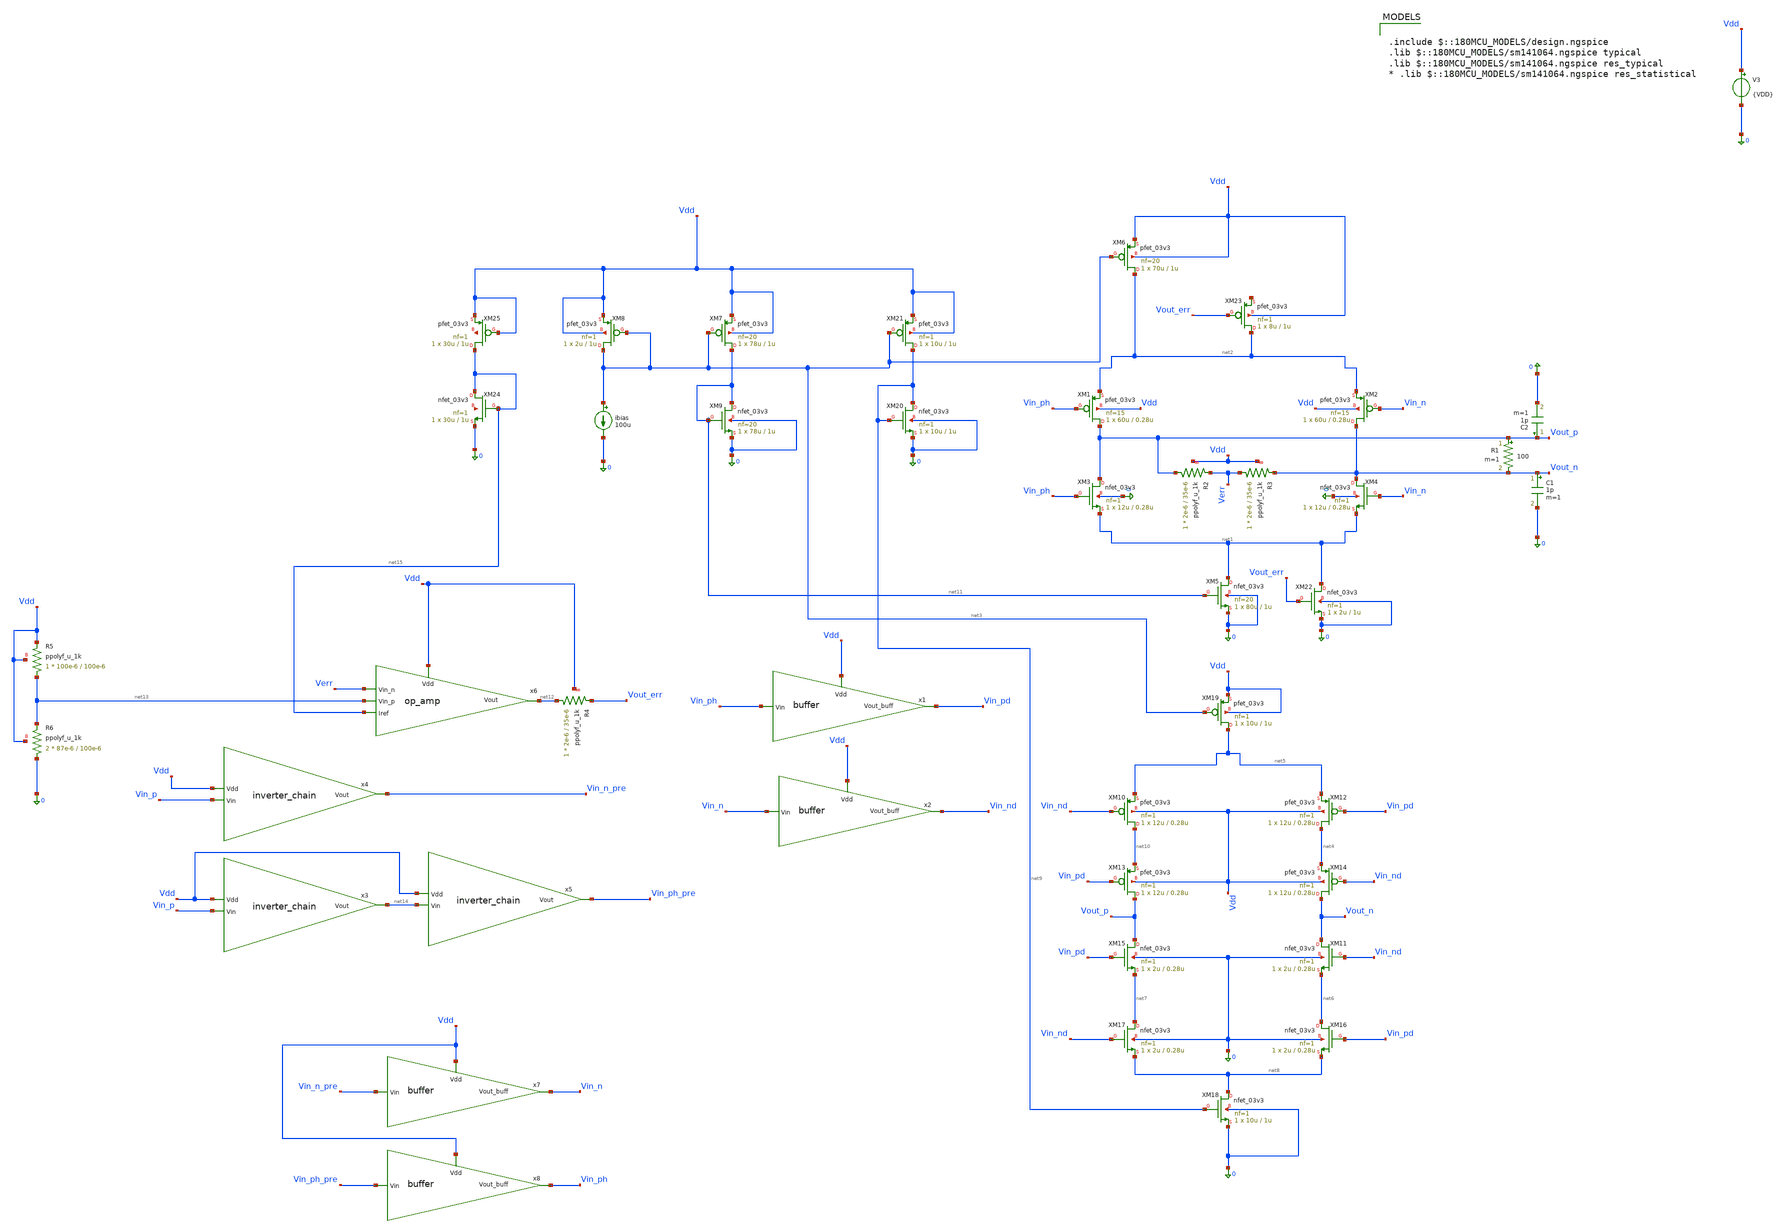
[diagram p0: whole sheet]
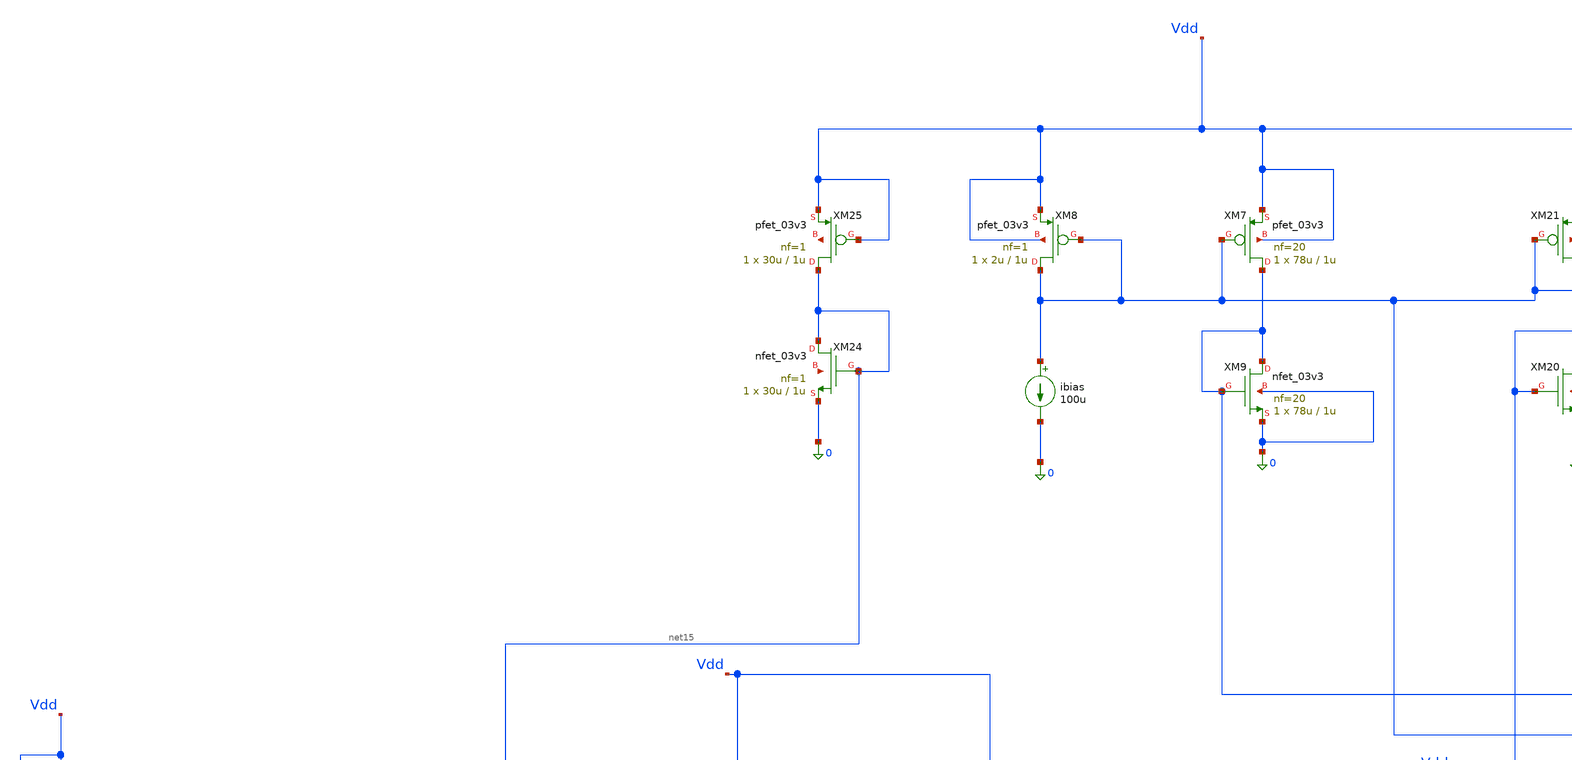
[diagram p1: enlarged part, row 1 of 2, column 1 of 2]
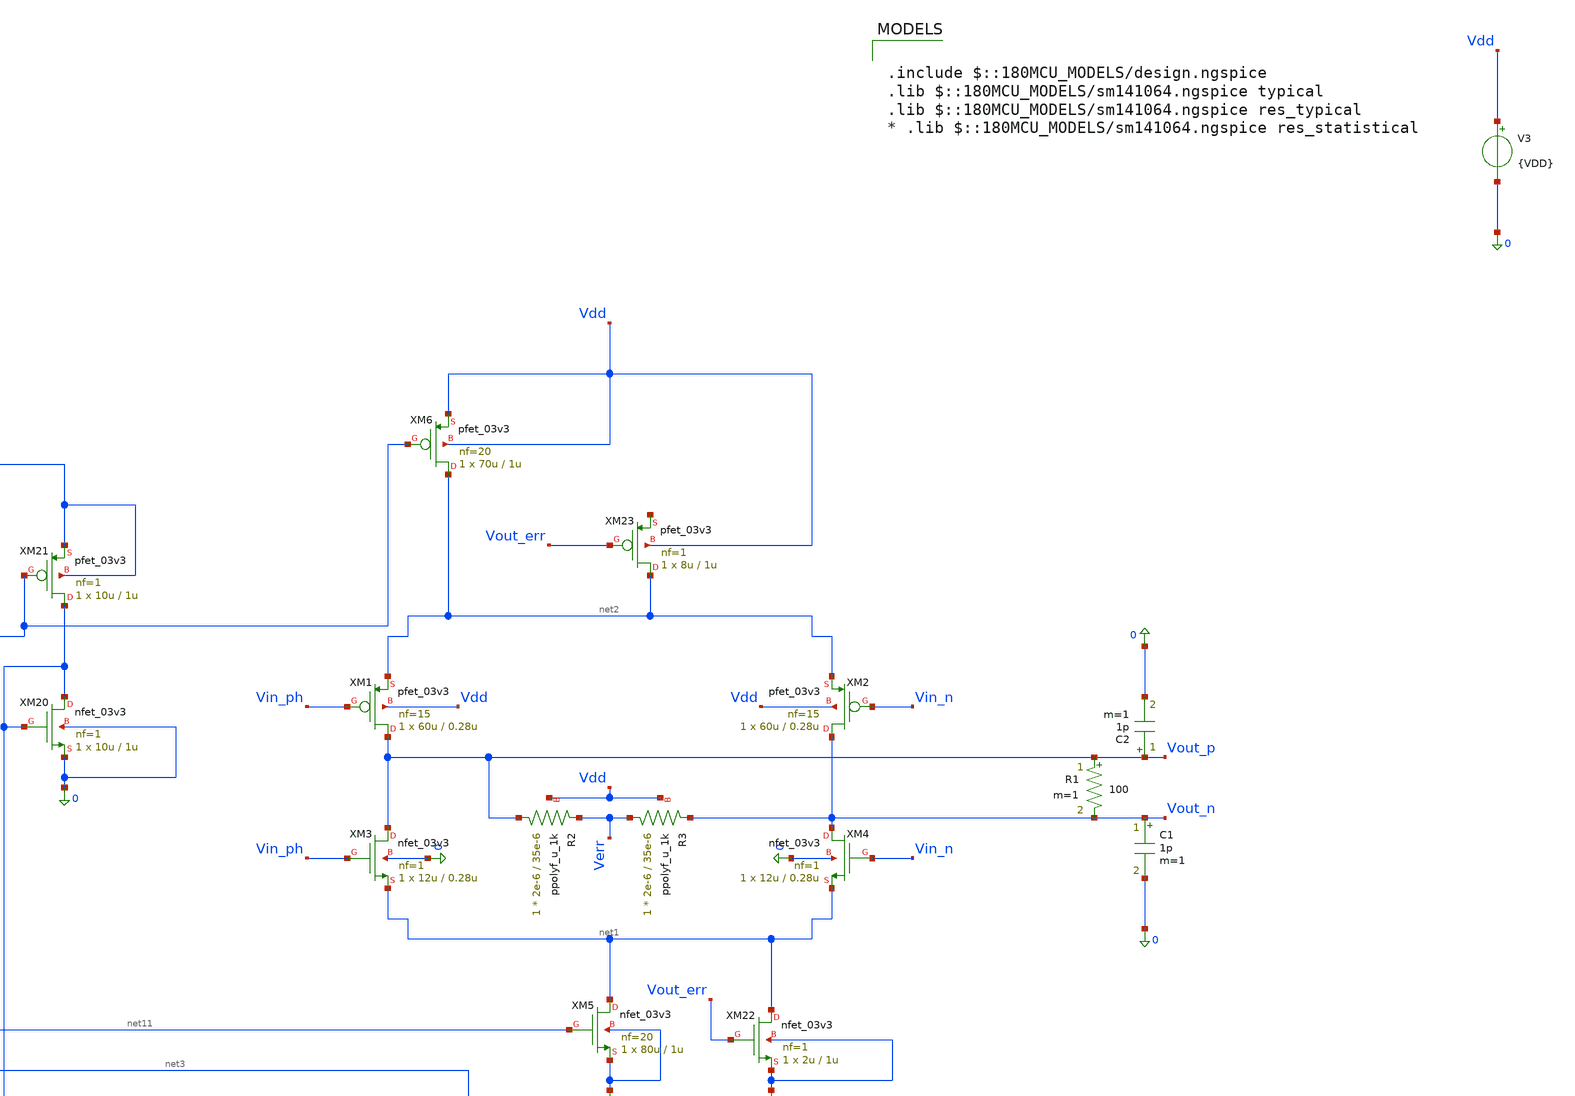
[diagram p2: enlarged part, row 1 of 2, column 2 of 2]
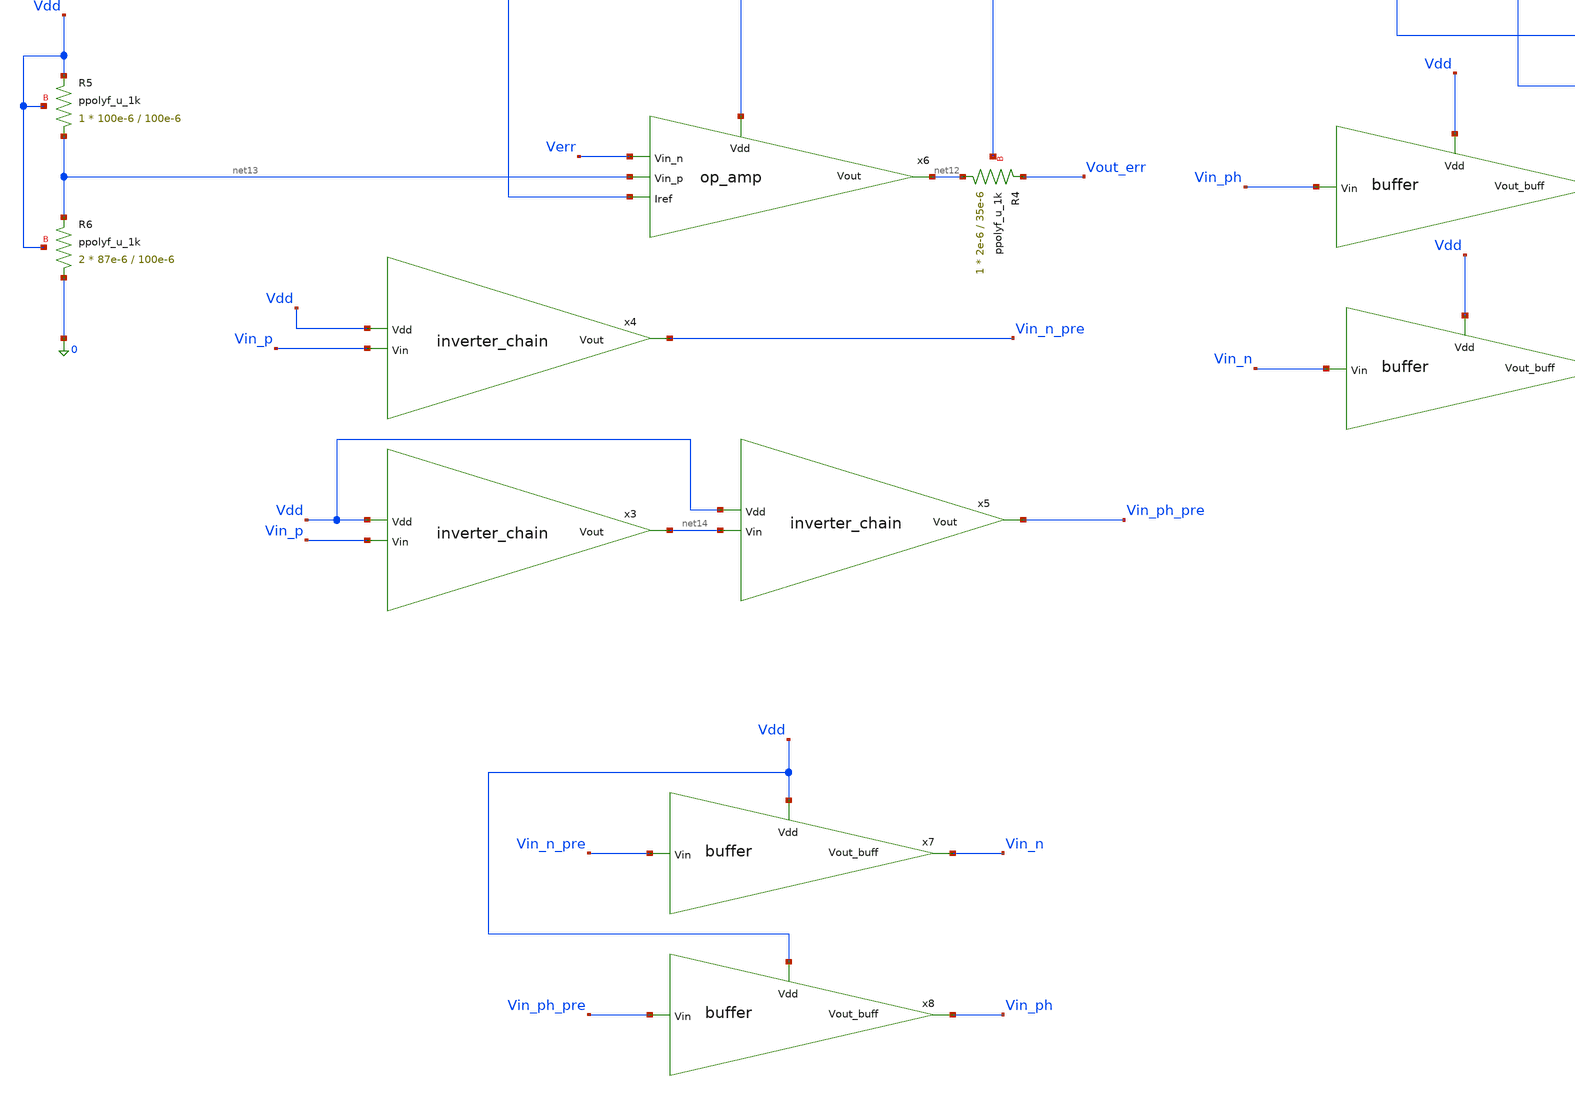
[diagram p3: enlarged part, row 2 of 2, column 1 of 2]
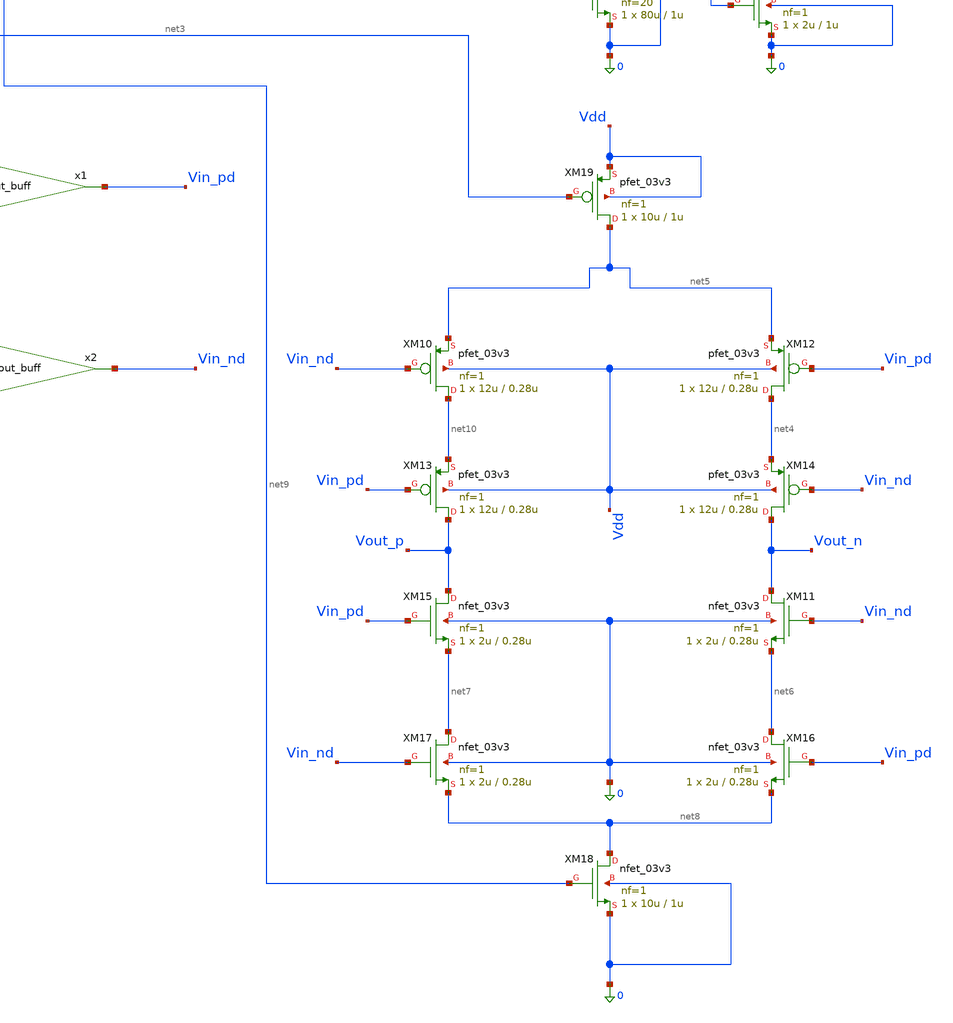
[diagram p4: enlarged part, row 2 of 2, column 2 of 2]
** sch_path: blocks/adc/lvds/lvds_testing.sch
**.subckt lvds_testing
R1 Vout_p Vout_n 100 m=1
V3 Vdd 0 {VDD}
XM1 Vout_p Vin_ph net2 Vdd pfet_03v3 L=0.28u W=60u nf=15 ad='int((nf+1)/2) * W/nf * 0.18u' as='int((nf+2)/2) * W/nf * 0.18u'
+ pd='2*int((nf+1)/2) * (W/nf + 0.18u)' ps='2*int((nf+2)/2) * (W/nf + 0.18u)' nrd='0.18u / W' nrs='0.18u / W'
+ sa=0 sb=0 sd=0 m=1
XM2 Vout_n Vin_n net2 Vdd pfet_03v3 L=0.28u W=60u nf=15 ad='int((nf+1)/2) * W/nf * 0.18u' as='int((nf+2)/2) * W/nf * 0.18u'
+ pd='2*int((nf+1)/2) * (W/nf + 0.18u)' ps='2*int((nf+2)/2) * (W/nf + 0.18u)' nrd='0.18u / W' nrs='0.18u / W'
+ sa=0 sb=0 sd=0 m=1
XM3 Vout_p Vin_ph net1 0 nfet_03v3 L=0.28u W=12u nf=1 ad='int((nf+1)/2) * W/nf * 0.18u' as='int((nf+2)/2) * W/nf * 0.18u'
+ pd='2*int((nf+1)/2) * (W/nf + 0.18u)' ps='2*int((nf+2)/2) * (W/nf + 0.18u)' nrd='0.18u / W' nrs='0.18u / W'
+ sa=0 sb=0 sd=0 m=1
XM4 Vout_n Vin_n net1 0 nfet_03v3 L=0.28u W=12u nf=1 ad='int((nf+1)/2) * W/nf * 0.18u' as='int((nf+2)/2) * W/nf * 0.18u'
+ pd='2*int((nf+1)/2) * (W/nf + 0.18u)' ps='2*int((nf+2)/2) * (W/nf + 0.18u)' nrd='0.18u / W' nrs='0.18u / W'
+ sa=0 sb=0 sd=0 m=1
XM5 net1 net11 0 0 nfet_03v3 L=1u W=80u nf=20 ad='int((nf+1)/2) * W/nf * 0.18u' as='int((nf+2)/2) * W/nf * 0.18u'
+ pd='2*int((nf+1)/2) * (W/nf + 0.18u)' ps='2*int((nf+2)/2) * (W/nf + 0.18u)' nrd='0.18u / W' nrs='0.18u / W'
+ sa=0 sb=0 sd=0 m=1
XM6 net2 net3 Vdd Vdd pfet_03v3 L=1u W=70u nf=20 ad='int((nf+1)/2) * W/nf * 0.18u' as='int((nf+2)/2) * W/nf * 0.18u'
+ pd='2*int((nf+1)/2) * (W/nf + 0.18u)' ps='2*int((nf+2)/2) * (W/nf + 0.18u)' nrd='0.18u / W' nrs='0.18u / W'
+ sa=0 sb=0 sd=0 m=1
XM8 net3 net3 Vdd Vdd pfet_03v3 L=1u W=2u nf=1 ad='int((nf+1)/2) * W/nf * 0.18u' as='int((nf+2)/2) * W/nf * 0.18u'
+ pd='2*int((nf+1)/2) * (W/nf + 0.18u)' ps='2*int((nf+2)/2) * (W/nf + 0.18u)' nrd='0.18u / W' nrs='0.18u / W'
+ sa=0 sb=0 sd=0 m=1
ibias net3 0 100u
XM10 net10 Vin_nd net5 Vdd pfet_03v3 L=0.28u W=12u nf=1 ad='int((nf+1)/2) * W/nf * 0.18u' as='int((nf+2)/2) * W/nf * 0.18u'
+ pd='2*int((nf+1)/2) * (W/nf + 0.18u)' ps='2*int((nf+2)/2) * (W/nf + 0.18u)' nrd='0.18u / W' nrs='0.18u / W'
+ sa=0 sb=0 sd=0 m=1
XM11 Vout_n Vin_nd net6 0 nfet_03v3 L=0.28u W=2u nf=1 ad='int((nf+1)/2) * W/nf * 0.18u' as='int((nf+2)/2) * W/nf * 0.18u'
+ pd='2*int((nf+1)/2) * (W/nf + 0.18u)' ps='2*int((nf+2)/2) * (W/nf + 0.18u)' nrd='0.18u / W' nrs='0.18u / W'
+ sa=0 sb=0 sd=0 m=1
XM12 net4 Vin_pd net5 Vdd pfet_03v3 L=0.28u W=12u nf=1 ad='int((nf+1)/2) * W/nf * 0.18u' as='int((nf+2)/2) * W/nf * 0.18u'
+ pd='2*int((nf+1)/2) * (W/nf + 0.18u)' ps='2*int((nf+2)/2) * (W/nf + 0.18u)' nrd='0.18u / W' nrs='0.18u / W'
+ sa=0 sb=0 sd=0 m=1
XM13 Vout_p Vin_pd net10 Vdd pfet_03v3 L=0.28u W=12u nf=1 ad='int((nf+1)/2) * W/nf * 0.18u' as='int((nf+2)/2) * W/nf * 0.18u'
+ pd='2*int((nf+1)/2) * (W/nf + 0.18u)' ps='2*int((nf+2)/2) * (W/nf + 0.18u)' nrd='0.18u / W' nrs='0.18u / W'
+ sa=0 sb=0 sd=0 m=1
XM14 Vout_n Vin_nd net4 Vdd pfet_03v3 L=0.28u W=12u nf=1 ad='int((nf+1)/2) * W/nf * 0.18u' as='int((nf+2)/2) * W/nf * 0.18u'
+ pd='2*int((nf+1)/2) * (W/nf + 0.18u)' ps='2*int((nf+2)/2) * (W/nf + 0.18u)' nrd='0.18u / W' nrs='0.18u / W'
+ sa=0 sb=0 sd=0 m=1
XM15 Vout_p Vin_pd net7 0 nfet_03v3 L=0.28u W=2u nf=1 ad='int((nf+1)/2) * W/nf * 0.18u' as='int((nf+2)/2) * W/nf * 0.18u'
+ pd='2*int((nf+1)/2) * (W/nf + 0.18u)' ps='2*int((nf+2)/2) * (W/nf + 0.18u)' nrd='0.18u / W' nrs='0.18u / W'
+ sa=0 sb=0 sd=0 m=1
XM16 net6 Vin_pd net8 0 nfet_03v3 L=0.28u W=2u nf=1 ad='int((nf+1)/2) * W/nf * 0.18u' as='int((nf+2)/2) * W/nf * 0.18u'
+ pd='2*int((nf+1)/2) * (W/nf + 0.18u)' ps='2*int((nf+2)/2) * (W/nf + 0.18u)' nrd='0.18u / W' nrs='0.18u / W'
+ sa=0 sb=0 sd=0 m=1
XM17 net7 Vin_nd net8 0 nfet_03v3 L=0.28u W=2u nf=1 ad='int((nf+1)/2) * W/nf * 0.18u' as='int((nf+2)/2) * W/nf * 0.18u'
+ pd='2*int((nf+1)/2) * (W/nf + 0.18u)' ps='2*int((nf+2)/2) * (W/nf + 0.18u)' nrd='0.18u / W' nrs='0.18u / W'
+ sa=0 sb=0 sd=0 m=1
XM18 net8 net9 0 0 nfet_03v3 L=1u W=10u nf=1 ad='int((nf+1)/2) * W/nf * 0.18u' as='int((nf+2)/2) * W/nf * 0.18u'
+ pd='2*int((nf+1)/2) * (W/nf + 0.18u)' ps='2*int((nf+2)/2) * (W/nf + 0.18u)' nrd='0.18u / W' nrs='0.18u / W'
+ sa=0 sb=0 sd=0 m=1
XM19 net5 net3 Vdd Vdd pfet_03v3 L=1u W=10u nf=1 ad='int((nf+1)/2) * W/nf * 0.18u' as='int((nf+2)/2) * W/nf * 0.18u'
+ pd='2*int((nf+1)/2) * (W/nf + 0.18u)' ps='2*int((nf+2)/2) * (W/nf + 0.18u)' nrd='0.18u / W' nrs='0.18u / W'
+ sa=0 sb=0 sd=0 m=1
XM21 net9 net3 Vdd Vdd pfet_03v3 L=1u W=10u nf=1 ad='int((nf+1)/2) * W/nf * 0.18u' as='int((nf+2)/2) * W/nf * 0.18u'
+ pd='2*int((nf+1)/2) * (W/nf + 0.18u)' ps='2*int((nf+2)/2) * (W/nf + 0.18u)' nrd='0.18u / W' nrs='0.18u / W'
+ sa=0 sb=0 sd=0 m=1
XM20 net9 net9 0 0 nfet_03v3 L=1u W=10u nf=1 ad='int((nf+1)/2) * W/nf * 0.18u' as='int((nf+2)/2) * W/nf * 0.18u'
+ pd='2*int((nf+1)/2) * (W/nf + 0.18u)' ps='2*int((nf+2)/2) * (W/nf + 0.18u)' nrd='0.18u / W' nrs='0.18u / W'
+ sa=0 sb=0 sd=0 m=1
C2 Vout_p 0 1p m=1
XR2 Vout_p Verr Vdd ppolyf_u_1k r_width=2e-6 r_length=35e-6 m=1
XR3 Verr Vout_n Vdd ppolyf_u_1k r_width=2e-6 r_length=35e-6 m=1
XM7 net11 net3 Vdd Vdd pfet_03v3 L=1u W=78u nf=20 ad='int((nf+1)/2) * W/nf * 0.18u' as='int((nf+2)/2) * W/nf * 0.18u'
+ pd='2*int((nf+1)/2) * (W/nf + 0.18u)' ps='2*int((nf+2)/2) * (W/nf + 0.18u)' nrd='0.18u / W' nrs='0.18u / W'
+ sa=0 sb=0 sd=0 m=1
XM9 net11 net11 0 0 nfet_03v3 L=1u W=78u nf=20 ad='int((nf+1)/2) * W/nf * 0.18u' as='int((nf+2)/2) * W/nf * 0.18u'
+ pd='2*int((nf+1)/2) * (W/nf + 0.18u)' ps='2*int((nf+2)/2) * (W/nf + 0.18u)' nrd='0.18u / W' nrs='0.18u / W'
+ sa=0 sb=0 sd=0 m=1
C1 Vout_n 0 1p m=1
x4 Vdd Vin_n_pre Vin_p inverter_chain
XM22 net1 Vout_err 0 0 nfet_03v3 L=1u W=2u nf=1 ad='int((nf+1)/2) * W/nf * 0.18u' as='int((nf+2)/2) * W/nf * 0.18u'
+ pd='2*int((nf+1)/2) * (W/nf + 0.18u)' ps='2*int((nf+2)/2) * (W/nf + 0.18u)' nrd='0.18u / W' nrs='0.18u / W'
+ sa=0 sb=0 sd=0 m=1
XM23 net2 Vout_err net16 Vdd pfet_03v3 L=1u W=8u nf=1 ad='int((nf+1)/2) * W/nf * 0.18u' as='int((nf+2)/2) * W/nf * 0.18u'
+ pd='2*int((nf+1)/2) * (W/nf + 0.18u)' ps='2*int((nf+2)/2) * (W/nf + 0.18u)' nrd='0.18u / W' nrs='0.18u / W'
+ sa=0 sb=0 sd=0 m=1
x3 Vdd net14 Vin_p inverter_chain
x5 Vdd Vin_ph_pre net14 inverter_chain
x7 Vdd Vin_n Vin_n_pre buffer
x8 Vdd Vin_ph Vin_ph_pre buffer
XM24 net15 net15 0 net17 nfet_03v3 L=1u W=30u nf=1 ad='int((nf+1)/2) * W/nf * 0.18u' as='int((nf+2)/2) * W/nf * 0.18u'
+ pd='2*int((nf+1)/2) * (W/nf + 0.18u)' ps='2*int((nf+2)/2) * (W/nf + 0.18u)' nrd='0.18u / W' nrs='0.18u / W'
+ sa=0 sb=0 sd=0 m=1
XM25 net15 Vdd Vdd net18 pfet_03v3 L=1u W=30u nf=1 ad='int((nf+1)/2) * W/nf * 0.18u' as='int((nf+2)/2) * W/nf * 0.18u'
+ pd='2*int((nf+1)/2) * (W/nf + 0.18u)' ps='2*int((nf+2)/2) * (W/nf + 0.18u)' nrd='0.18u / W' nrs='0.18u / W'
+ sa=0 sb=0 sd=0 m=1
x1 Vdd Vin_pd Vin_ph buffer
x2 Vdd Vin_nd Vin_n buffer
XR4 net12 Vout_err Vdd ppolyf_u_1k r_width=2e-6 r_length=35e-6 m=1
x6 Vdd net12 Verr net13 net15 op_amp
XR5 net13 Vdd Vdd ppolyf_u_1k r_width=100e-6 r_length=100e-6 m=1
XR6 0 net13 Vdd ppolyf_u_1k r_width=87e-6 r_length=100e-6 m=2
**** begin user architecture code


.param VDD=3.3
.param VCM=1.2

* Temperature parameter used by .options
.param TEMP=27
.options temp={TEMP}

* 2 Gbps
.param UI=500p
.param TR=20p
.param SEED=11

* Jitter setting
* Use 0p for no jitter, e.g. .param TJPP=0p
.param TJPP=0p

* ============================================================
* Internal pseudo-random data generation
* ============================================================

.func frac(x) {x - floor(x)}
.func rand01(n) {frac(sin((n + 1 + SEED)*12.9898)*43758.5453123)}
.func rand01j(n) {frac(sin((n + 1 + SEED)*78.233)*24634.6345)}
.func rbit(n) {floor(2*rand01(n))}
.func jitter(n) {(rand01j(n)-0.5)*TJPP}
.func edge(x) {0.5*(1 + tanh(x/(TR/10)))}
.func data_bit(t) {rbit(floor(t/UI)-1)+(rbit(floor(t/UI))-rbit(floor(t/UI)-1))*edge(t-floor(t/UI)*UI-jitter(floor(t/UI)))}

* ============================================================
* Behavioral input sources
* Remove/disable old PULSE sources connected to vin_p/vin_n.
* ============================================================

Bvinp vin_p 0 V={VDD*data_bit(time)}



.control
set filetype=ascii
set wr_singlescale
set numdgt=12

* Folder for output data files
shell rm /foss/designs/trans_testing/lvds_testing/lvds_eye_temp_m40.txt
shell rm /foss/designs/trans_testing/lvds_testing/lvds_eye_temp_27.txt
shell rm /foss/designs/trans_testing/lvds_testing/lvds_eye_temp_125.txt

* ============================================================
* Temperature = -40 C
* ============================================================

alterparam TEMP = -40
set temp=-40
reset
save v(vin_p) v(vin_n) v(vout_p) v(vout_n) v(Vin_ph) v(Vin_nd) v(Vin_pd) v(Vout_err)

tran 2p 200n 0 2p

let vod = v(vout_p)-v(vout_n)
let vcm_out = (v(vout_p)+v(vout_n))/2
let vod_abs = abs(vod)
let id_p = @m.xm5.m0[id]
let id_n = @m.xm6.m0[id]

plot v(Vin_n) v(Vin_nd)
plot v(Vin_pd) v(Vin_ph)
plot id_p id_n
plot v(Vout_err)


wrdata /foss/designs/trans_testing/lvds_testing/lvds_eye_temp_m40.txt v(vin_p) v(vin_n) v(vout_p)
+ v(vout_n) vod vcm_out


meas tran td_pd_rise TRIG v(vin_ph) VAL=1.65 RISE=10 TARG v(vin_pd) VAL=1.65 RISE=10
meas tran td_pd_fall TRIG v(vin_ph) VAL=1.65 FALL=10 TARG v(vin_pd) VAL=1.65 FALL=10

meas tran td_nd_rise TRIG v(vin_n) VAL=1.65 RISE=10 TARG v(vin_nd) VAL=1.65 RISE=10
meas tran td_nd_fall TRIG v(vin_n) VAL=1.65 FALL=10 TARG v(vin_nd) VAL=1.65 FALL=10

* 50% complementary skew
meas tran skew_ph_rise_n_fall TRIG v(vin_ph) VAL=1.65 RISE=10 TARG v(vin_n)  VAL=1.65 FALL=10
meas tran skew_ph_fall_n_rise TRIG v(vin_ph) VAL=1.65 FALL=10 TARG v(vin_n)  VAL=1.65 RISE=10

* Edge times
meas tran tr_ph TRIG v(vin_ph) VAL=0.33 RISE=10 TARG v(vin_ph) VAL=2.97 RISE=10
meas tran tf_ph TRIG v(vin_ph) VAL=2.97 FALL=10 TARG v(vin_ph) VAL=0.33 FALL=10

meas tran tr_n  TRIG v(vin_n)  VAL=0.33 RISE=10 TARG v(vin_n)  VAL=2.97 RISE=10
meas tran tf_n  TRIG v(vin_n)  VAL=2.97 FALL=10 TARG v(vin_n)  VAL=0.33 FALL=10
* ============================================================
* Temperature = 27 C
* ============================================================

alterparam TEMP = 27
set temp=27
reset
save v(vin_p) v(vin_n) v(vout_p) v(vout_n) v(Vin_ph) v(Vin_nd) v(Vin_pd) v(Vout_err)

tran 2p 200n 0 2p

let vod = v(vout_p)-v(vout_n)
let vcm_out = (v(vout_p)+v(vout_n))/2
let vod_abs = abs(vod)
let id_p = @m.xm5.m0[id]
let id_n = @m.xm6.m0[id]
plot v(Vin_n) v(Vin_nd)
plot v(Vin_pd) v(Vin_ph)
plot id_p id_n
v(Vout_err)

wrdata /foss/designs/trans_testing/lvds_testing/lvds_eye_temp_27.txt v(vin_p) v(vin_n) v(vout_p)
+ v(vout_n) vod vcm_out


meas tran td_pd_rise TRIG v(vin_ph) VAL=1.65 RISE=10 TARG v(vin_pd) VAL=1.65 RISE=10
meas tran td_pd_fall TRIG v(vin_ph) VAL=1.65 FALL=10 TARG v(vin_pd) VAL=1.65 FALL=10

meas tran td_nd_rise TRIG v(vin_n) VAL=1.65 RISE=10 TARG v(vin_nd) VAL=1.65 RISE=10
meas tran td_nd_fall TRIG v(vin_n) VAL=1.65 FALL=10 TARG v(vin_nd) VAL=1.65 FALL=10


* 50% complementary skew
meas tran skew_ph_rise_n_fall TRIG v(vin_ph) VAL=1.65 RISE=10 TARG v(vin_n)  VAL=1.65 FALL=10
meas tran skew_ph_fall_n_rise TRIG v(vin_ph) VAL=1.65 FALL=10 TARG v(vin_n)  VAL=1.65 RISE=10

* Edge times
meas tran tr_ph TRIG v(vin_ph) VAL=0.33 RISE=10 TARG v(vin_ph) VAL=2.97 RISE=10
meas tran tf_ph TRIG v(vin_ph) VAL=2.97 FALL=10 TARG v(vin_ph) VAL=0.33 FALL=10

meas tran tr_n  TRIG v(vin_n)  VAL=0.33 RISE=10 TARG v(vin_n)  VAL=2.97 RISE=10
meas tran tf_n  TRIG v(vin_n)  VAL=2.97 FALL=10 TARG v(vin_n)  VAL=0.33 FALL=10
* ============================================================
* Temperature = 125 C
* ============================================================

alterparam TEMP = 125
set temp=125
reset
save v(vin_p) v(vin_n) v(vout_p) v(vout_n) v(Vin_ph) v(Vin_nd) v(Vin_pd) v(Vout_err)

tran 2p 200n 0 2p

let vod = v(vout_p)-v(vout_n)
let vcm_out = (v(vout_p)+v(vout_n))/2
let vod_abs = abs(vod)
plot v(Vin_n) v(Vin_nd)
plot v(Vin_pd) v(Vin_ph)
v(Vout_err)

wrdata /foss/designs/trans_testing/lvds_testing/lvds_eye_temp_125.txt v(vin_p) v(vin_n) v(vout_p)
+ v(vout_n) vod vcm_out


meas tran td_pd_rise TRIG v(vin_ph) VAL=1.65 RISE=10 TARG v(vin_pd) VAL=1.65 RISE=10
meas tran td_pd_fall TRIG v(vin_ph) VAL=1.65 FALL=10 TARG v(vin_pd) VAL=1.65 FALL=10

meas tran td_nd_rise TRIG v(vin_n) VAL=1.65 RISE=10 TARG v(vin_nd) VAL=1.65 RISE=10
meas tran td_nd_fall TRIG v(vin_n) VAL=1.65 FALL=10 TARG v(vin_nd) VAL=1.65 FALL=10

* 50% complementary skew
meas tran skew_ph_rise_n_fall TRIG v(vin_ph) VAL=1.65 RISE=10 TARG v(vin_n)  VAL=1.65 FALL=10
meas tran skew_ph_fall_n_rise TRIG v(vin_ph) VAL=1.65 FALL=10 TARG v(vin_n)  VAL=1.65 RISE=10

* Edge times
meas tran tr_ph TRIG v(vin_ph) VAL=0.33 RISE=10 TARG v(vin_ph) VAL=2.97 RISE=10
meas tran tf_ph TRIG v(vin_ph) VAL=2.97 FALL=10 TARG v(vin_ph) VAL=0.33 FALL=10

meas tran tr_n  TRIG v(vin_n)  VAL=0.33 RISE=10 TARG v(vin_n)  VAL=2.97 RISE=10
meas tran tf_n  TRIG v(vin_n)  VAL=2.97 FALL=10 TARG v(vin_n)  VAL=0.33 FALL=10
.endc



.include $::180MCU_MODELS/design.ngspice
.lib $::180MCU_MODELS/sm141064.ngspice typical
.lib $::180MCU_MODELS/sm141064.ngspice res_typical
* .lib $::180MCU_MODELS/sm141064.ngspice res_statistical

**** end user architecture code
**.ends
.end
